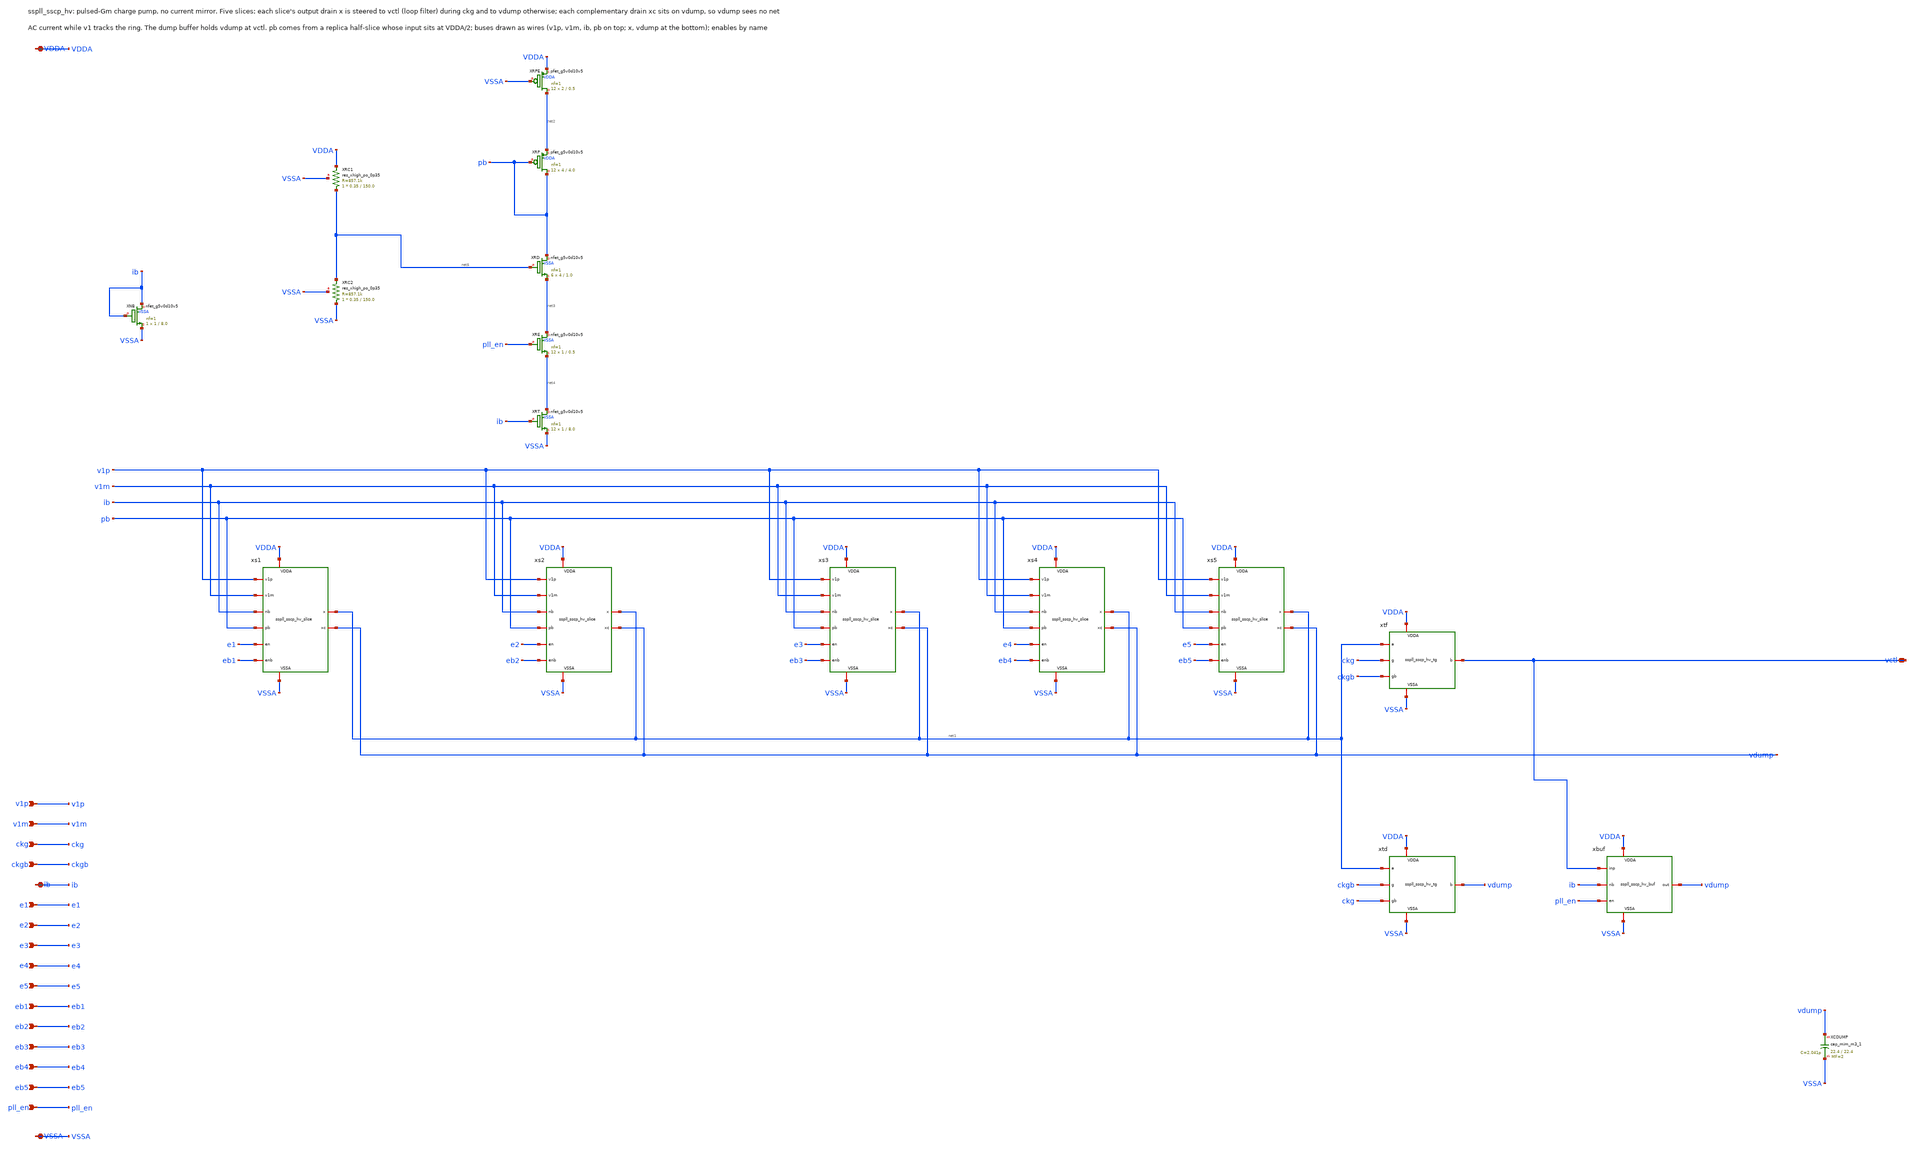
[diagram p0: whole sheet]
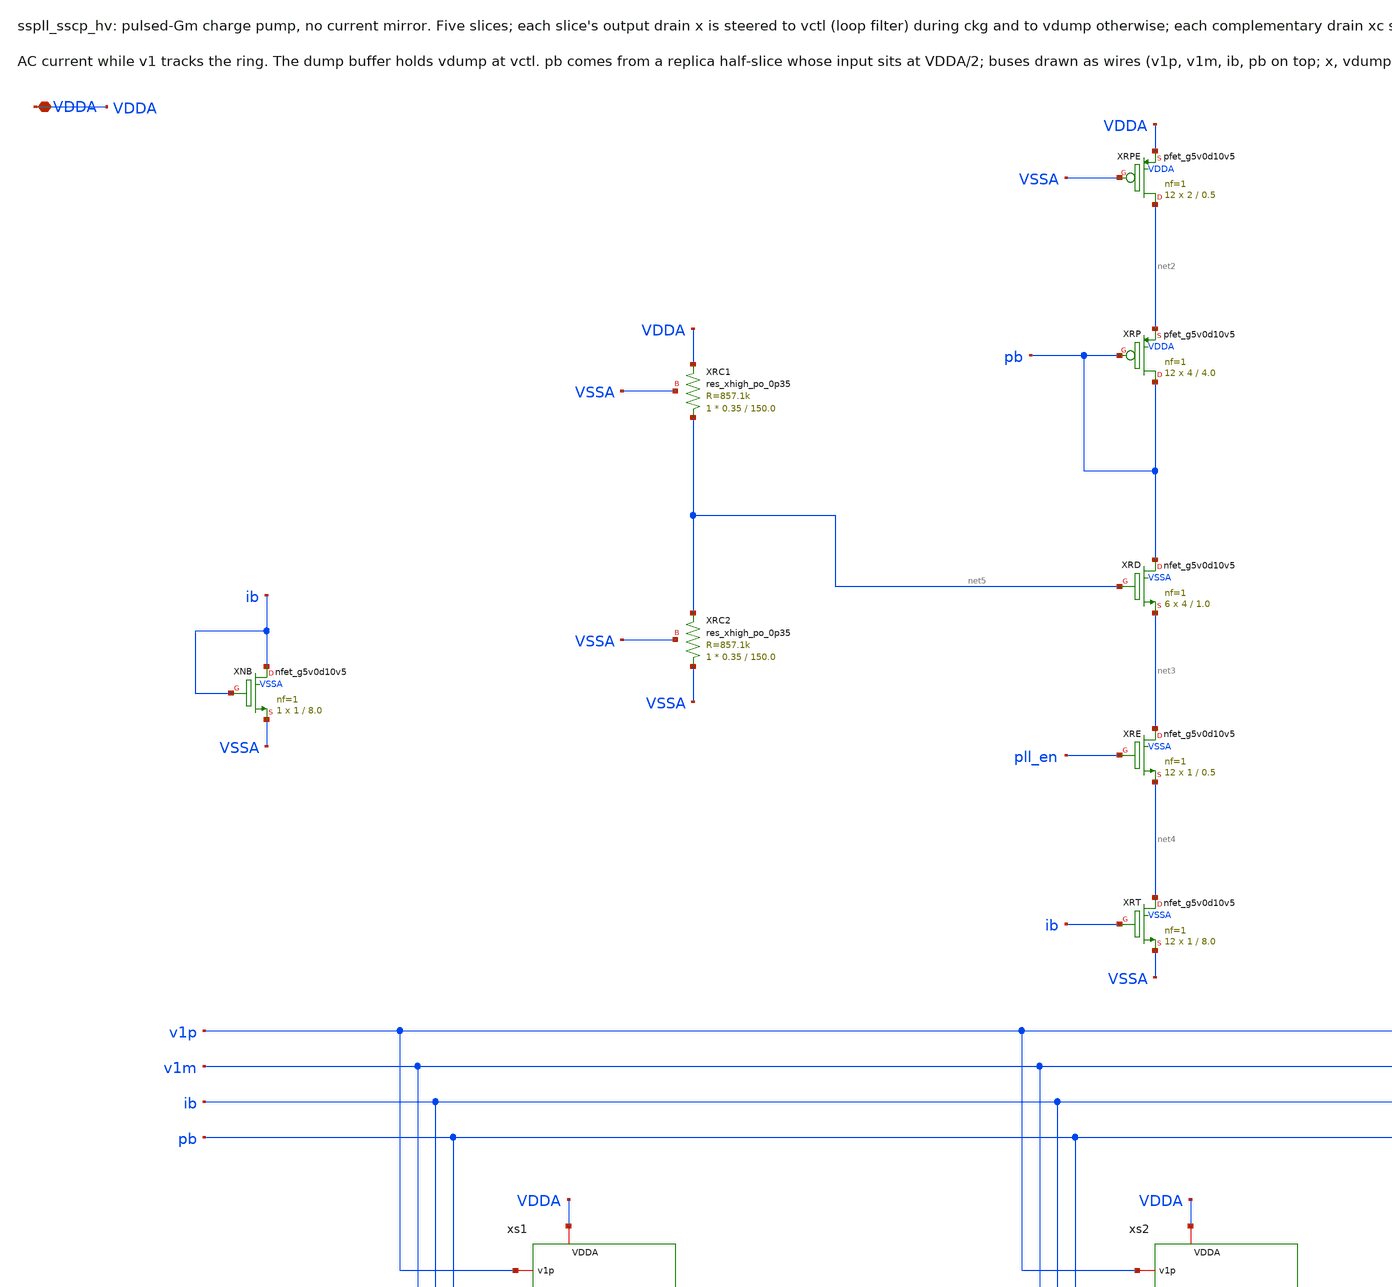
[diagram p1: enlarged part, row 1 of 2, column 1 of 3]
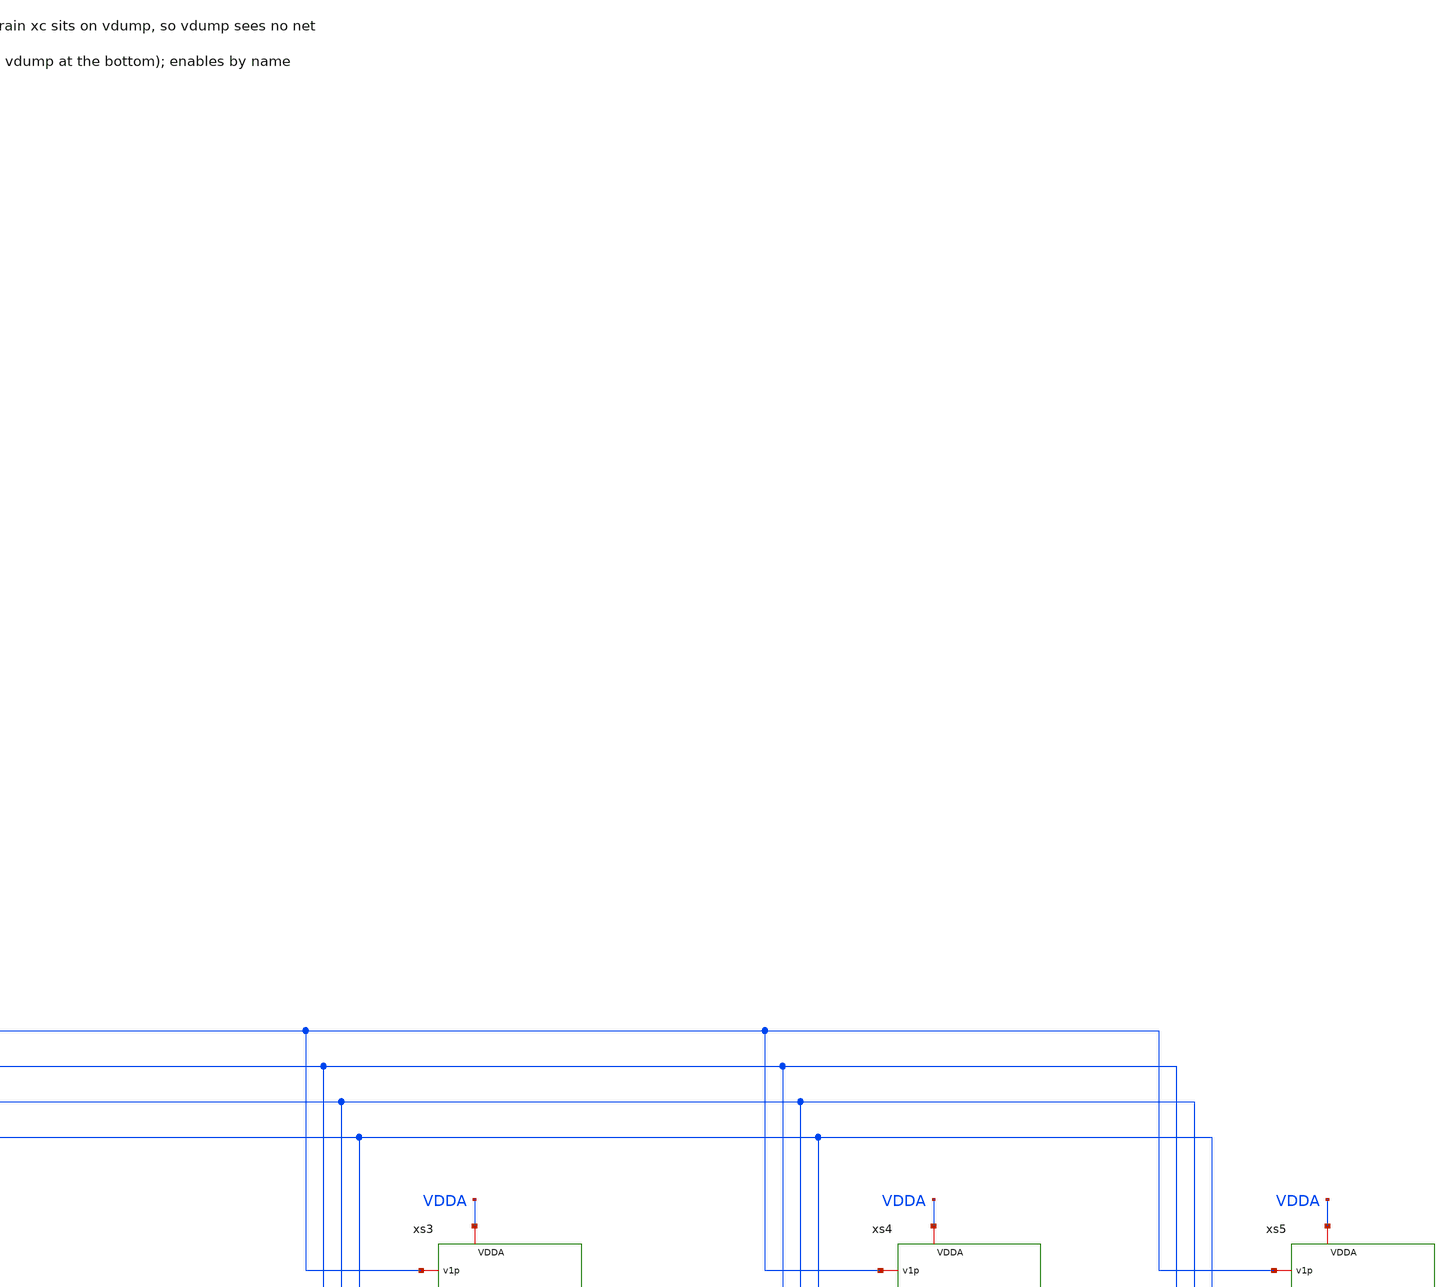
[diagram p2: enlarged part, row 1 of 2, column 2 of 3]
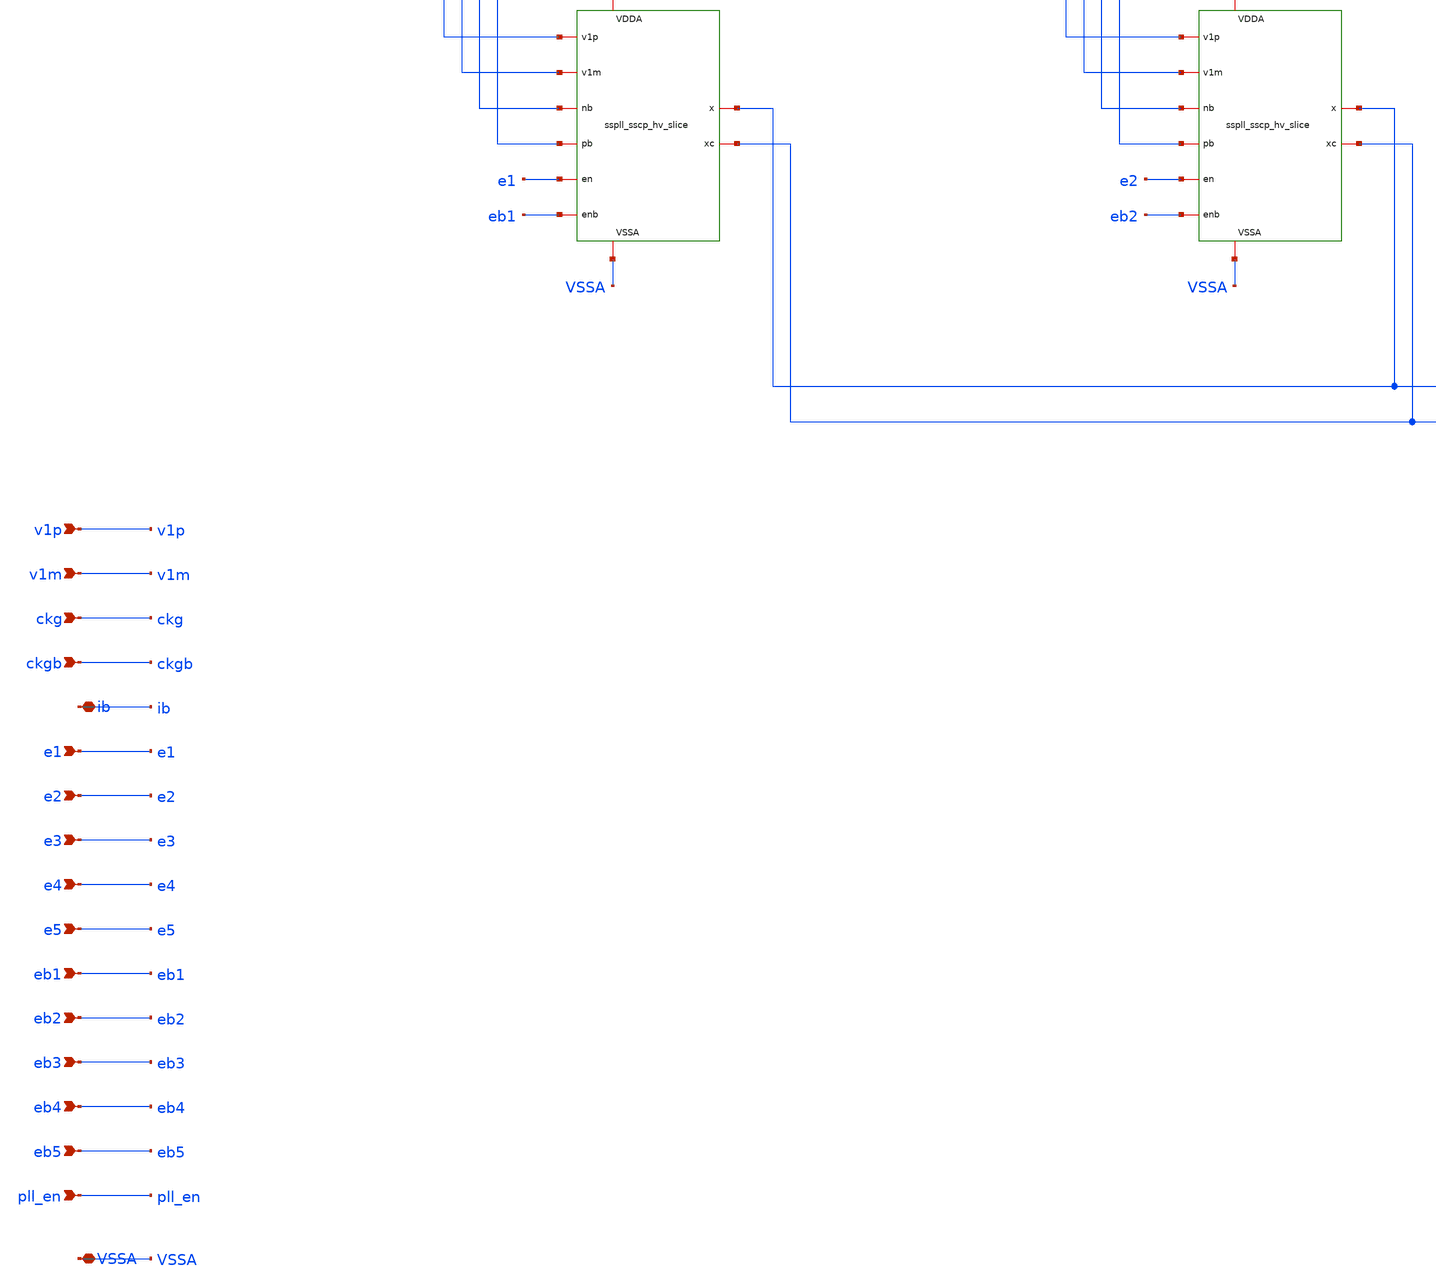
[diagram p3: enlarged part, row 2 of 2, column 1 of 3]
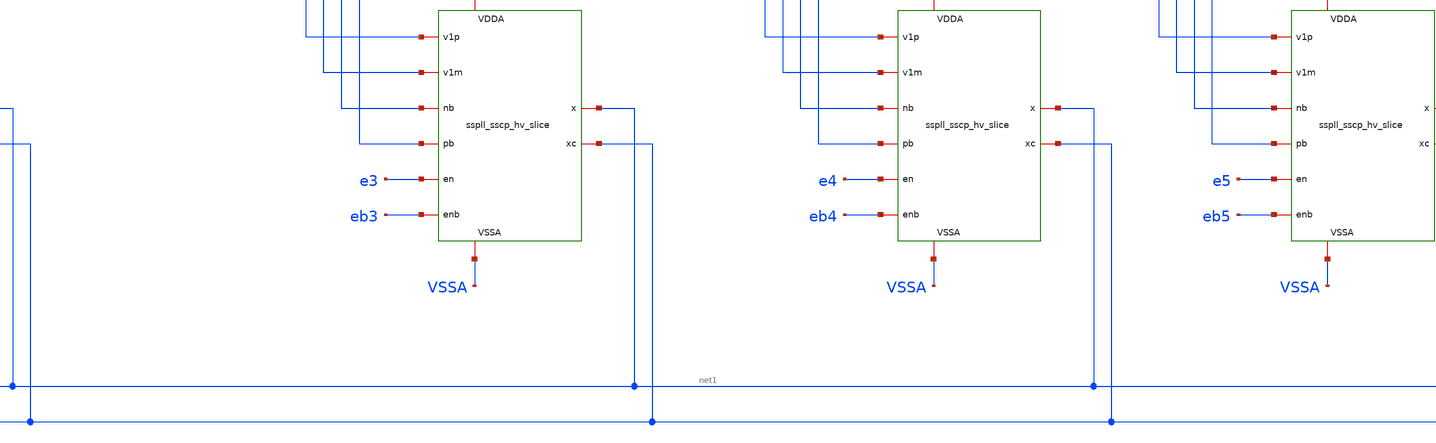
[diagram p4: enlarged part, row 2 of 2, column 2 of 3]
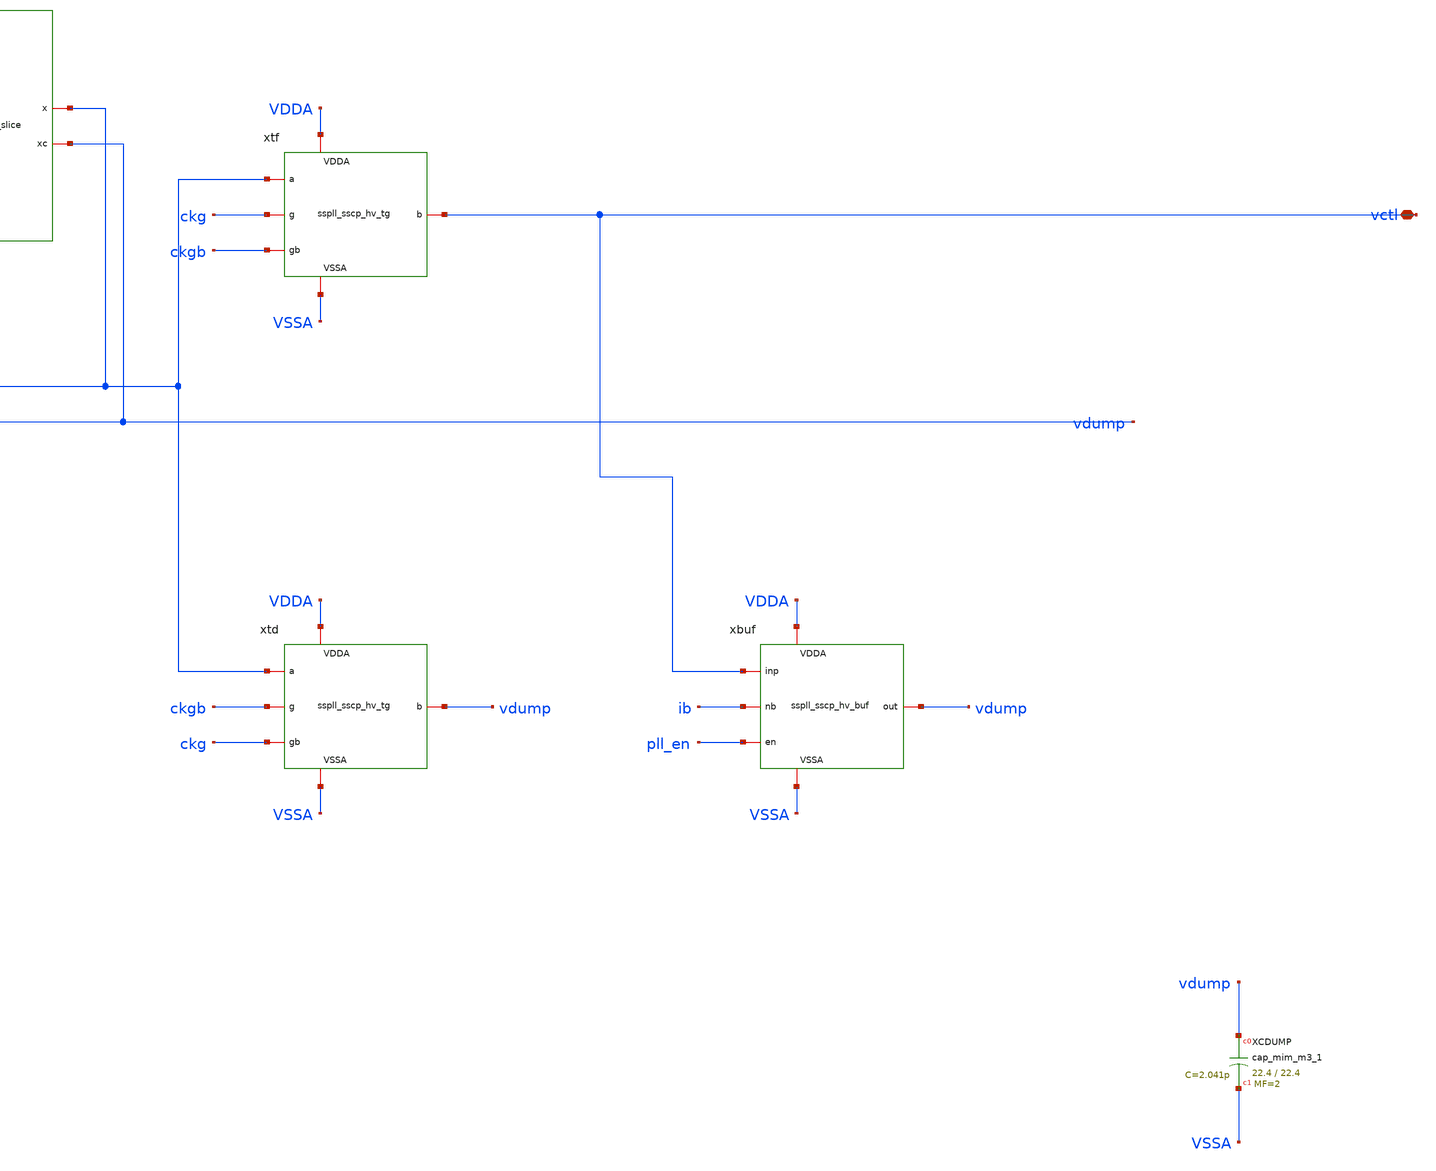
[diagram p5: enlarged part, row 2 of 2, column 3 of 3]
** sch_path: xschem/sscp_hv/sspll_sscp_hv.sch
**.subckt sspll_sscp_hv vctl v1p v1m ckg ckgb ib e1 e2 e3 e4 e5 eb1 eb2 eb3 eb4 eb5 pll_en VDDA VSSA
*.iopin vctl
*.ipin v1p
*.ipin v1m
*.ipin ckg
*.ipin ckgb
*.iopin ib
*.ipin e1
*.ipin e2
*.ipin e3
*.ipin e4
*.ipin e5
*.ipin eb1
*.ipin eb2
*.ipin eb3
*.ipin eb4
*.ipin eb5
*.ipin pll_en
*.iopin VDDA
*.iopin VSSA
xs1 v1p v1m ib pb e1 eb1 net1 vdump VDDA VSSA sspll_sscp_hv_slice
xs2 v1p v1m ib pb e2 eb2 net1 vdump VDDA VSSA sspll_sscp_hv_slice
xs3 v1p v1m ib pb e3 eb3 net1 vdump VDDA VSSA sspll_sscp_hv_slice
xs4 v1p v1m ib pb e4 eb4 net1 vdump VDDA VSSA sspll_sscp_hv_slice
xs5 v1p v1m ib pb e5 eb5 net1 vdump VDDA VSSA sspll_sscp_hv_slice
xtf net1 ckg ckgb vctl VDDA VSSA sspll_sscp_hv_tg
xtd net1 ckgb ckg vdump VDDA VSSA sspll_sscp_hv_tg
xbuf vctl ib pll_en vdump VDDA VSSA sspll_sscp_hv_buf
XXCDUMP vdump VSSA sky130_fd_pr__cap_mim_m3_1 W=22.4 L=22.4 MF=2 m=2
XXNB ib ib VSSA VSSA sky130_fd_pr__nfet_g5v0d10v5 L=8.0 W=1 nf=1 ad='int((nf+1)/2) * W/nf * 0.29' as='int((nf+2)/2) * W/nf * 0.29'
+ pd='2*int((nf+1)/2) * (W/nf + 0.29)' ps='2*int((nf+2)/2) * (W/nf + 0.29)' nrd='0.29 / W' nrs='0.29 / W'
+ sa=0 sb=0 sd=0 mult=1 m=1
XXRPE net2 VSSA VDDA VDDA sky130_fd_pr__pfet_g5v0d10v5 L=0.5 W=2 nf=1 ad='int((nf+1)/2) * W/nf * 0.29'
+ as='int((nf+2)/2) * W/nf * 0.29' pd='2*int((nf+1)/2) * (W/nf + 0.29)' ps='2*int((nf+2)/2) * (W/nf + 0.29)'
+ nrd='0.29 / W' nrs='0.29 / W' sa=0 sb=0 sd=0 mult=12 m=12
XXRP pb pb net2 VDDA sky130_fd_pr__pfet_g5v0d10v5 L=4.0 W=4 nf=1 ad='int((nf+1)/2) * W/nf * 0.29' as='int((nf+2)/2) * W/nf * 0.29'
+ pd='2*int((nf+1)/2) * (W/nf + 0.29)' ps='2*int((nf+2)/2) * (W/nf + 0.29)' nrd='0.29 / W' nrs='0.29 / W'
+ sa=0 sb=0 sd=0 mult=12 m=12
XXRD pb net5 net3 VSSA sky130_fd_pr__nfet_g5v0d10v5 L=1.0 W=4 nf=1 ad='int((nf+1)/2) * W/nf * 0.29' as='int((nf+2)/2) * W/nf * 0.29'
+ pd='2*int((nf+1)/2) * (W/nf + 0.29)' ps='2*int((nf+2)/2) * (W/nf + 0.29)' nrd='0.29 / W' nrs='0.29 / W'
+ sa=0 sb=0 sd=0 mult=6 m=6
XXRE net3 pll_en net4 VSSA sky130_fd_pr__nfet_g5v0d10v5 L=0.5 W=1 nf=1 ad='int((nf+1)/2) * W/nf * 0.29'
+ as='int((nf+2)/2) * W/nf * 0.29' pd='2*int((nf+1)/2) * (W/nf + 0.29)' ps='2*int((nf+2)/2) * (W/nf + 0.29)'
+ nrd='0.29 / W' nrs='0.29 / W' sa=0 sb=0 sd=0 mult=12 m=12
XXRT net4 ib VSSA VSSA sky130_fd_pr__nfet_g5v0d10v5 L=8.0 W=1 nf=1 ad='int((nf+1)/2) * W/nf * 0.29' as='int((nf+2)/2) * W/nf * 0.29'
+ pd='2*int((nf+1)/2) * (W/nf + 0.29)' ps='2*int((nf+2)/2) * (W/nf + 0.29)' nrd='0.29 / W' nrs='0.29 / W'
+ sa=0 sb=0 sd=0 mult=12 m=12
XXRC1 net5 VDDA VSSA sky130_fd_pr__res_xhigh_po_0p35 L=150.0 mult=1 m=1
XXRC2 VSSA net5 VSSA sky130_fd_pr__res_xhigh_po_0p35 L=150.0 mult=1 m=1
**.ends

* expanding   symbol:  sspll_sscp_hv_slice.sym # of pins=10
** sym_path: xschem/sscp_hv/sspll_sscp_hv_slice.sym
** sch_path: xschem/sscp_hv/sspll_sscp_hv_slice.sch
.subckt sspll_sscp_hv_slice v1p v1m nb pb en enb x xc VDDA VSSA
*.ipin v1p
*.ipin v1m
*.ipin nb
*.ipin pb
*.ipin en
*.ipin enb
*.iopin x
*.iopin xc
*.iopin VDDA
*.iopin VSSA
XXPE1 net1 enb VDDA VDDA sky130_fd_pr__pfet_g5v0d10v5 L=0.5 W=2 nf=1 ad='int((nf+1)/2) * W/nf * 0.29'
+ as='int((nf+2)/2) * W/nf * 0.29' pd='2*int((nf+1)/2) * (W/nf + 0.29)' ps='2*int((nf+2)/2) * (W/nf + 0.29)'
+ nrd='0.29 / W' nrs='0.29 / W' sa=0 sb=0 sd=0 mult=2 m=2
XXPE2 net2 enb VDDA VDDA sky130_fd_pr__pfet_g5v0d10v5 L=0.5 W=2 nf=1 ad='int((nf+1)/2) * W/nf * 0.29'
+ as='int((nf+2)/2) * W/nf * 0.29' pd='2*int((nf+1)/2) * (W/nf + 0.29)' ps='2*int((nf+2)/2) * (W/nf + 0.29)'
+ nrd='0.29 / W' nrs='0.29 / W' sa=0 sb=0 sd=0 mult=2 m=2
XXPC xc pb net1 VDDA sky130_fd_pr__pfet_g5v0d10v5 L=4.0 W=4 nf=1 ad='int((nf+1)/2) * W/nf * 0.29' as='int((nf+2)/2) * W/nf * 0.29'
+ pd='2*int((nf+1)/2) * (W/nf + 0.29)' ps='2*int((nf+2)/2) * (W/nf + 0.29)' nrd='0.29 / W' nrs='0.29 / W'
+ sa=0 sb=0 sd=0 mult=2 m=2
XXPX x pb net2 VDDA sky130_fd_pr__pfet_g5v0d10v5 L=4.0 W=4 nf=1 ad='int((nf+1)/2) * W/nf * 0.29' as='int((nf+2)/2) * W/nf * 0.29'
+ pd='2*int((nf+1)/2) * (W/nf + 0.29)' ps='2*int((nf+2)/2) * (W/nf + 0.29)' nrd='0.29 / W' nrs='0.29 / W'
+ sa=0 sb=0 sd=0 mult=2 m=2
XXN1 xc v1p net3 VSSA sky130_fd_pr__nfet_g5v0d10v5 L=1.0 W=4 nf=1 ad='int((nf+1)/2) * W/nf * 0.29' as='int((nf+2)/2) * W/nf * 0.29'
+ pd='2*int((nf+1)/2) * (W/nf + 0.29)' ps='2*int((nf+2)/2) * (W/nf + 0.29)' nrd='0.29 / W' nrs='0.29 / W'
+ sa=0 sb=0 sd=0 mult=1 m=1
XXN2 x v1m net4 VSSA sky130_fd_pr__nfet_g5v0d10v5 L=1.0 W=4 nf=1 ad='int((nf+1)/2) * W/nf * 0.29' as='int((nf+2)/2) * W/nf * 0.29'
+ pd='2*int((nf+1)/2) * (W/nf + 0.29)' ps='2*int((nf+2)/2) * (W/nf + 0.29)' nrd='0.29 / W' nrs='0.29 / W'
+ sa=0 sb=0 sd=0 mult=1 m=1
xrs net3 net4 VSSA sspll_sscp_hv_rs
XXE1 net3 en net5 VSSA sky130_fd_pr__nfet_g5v0d10v5 L=0.5 W=1 nf=1 ad='int((nf+1)/2) * W/nf * 0.29' as='int((nf+2)/2) * W/nf * 0.29'
+ pd='2*int((nf+1)/2) * (W/nf + 0.29)' ps='2*int((nf+2)/2) * (W/nf + 0.29)' nrd='0.29 / W' nrs='0.29 / W'
+ sa=0 sb=0 sd=0 mult=2 m=2
XXE2 net4 en net6 VSSA sky130_fd_pr__nfet_g5v0d10v5 L=0.5 W=1 nf=1 ad='int((nf+1)/2) * W/nf * 0.29' as='int((nf+2)/2) * W/nf * 0.29'
+ pd='2*int((nf+1)/2) * (W/nf + 0.29)' ps='2*int((nf+2)/2) * (W/nf + 0.29)' nrd='0.29 / W' nrs='0.29 / W'
+ sa=0 sb=0 sd=0 mult=2 m=2
XXT1 net5 nb VSSA VSSA sky130_fd_pr__nfet_g5v0d10v5 L=8.0 W=1 nf=1 ad='int((nf+1)/2) * W/nf * 0.29' as='int((nf+2)/2) * W/nf * 0.29'
+ pd='2*int((nf+1)/2) * (W/nf + 0.29)' ps='2*int((nf+2)/2) * (W/nf + 0.29)' nrd='0.29 / W' nrs='0.29 / W'
+ sa=0 sb=0 sd=0 mult=2 m=2
XXT2 net6 nb VSSA VSSA sky130_fd_pr__nfet_g5v0d10v5 L=8.0 W=1 nf=1 ad='int((nf+1)/2) * W/nf * 0.29' as='int((nf+2)/2) * W/nf * 0.29'
+ pd='2*int((nf+1)/2) * (W/nf + 0.29)' ps='2*int((nf+2)/2) * (W/nf + 0.29)' nrd='0.29 / W' nrs='0.29 / W'
+ sa=0 sb=0 sd=0 mult=2 m=2
.ends


* expanding   symbol:  sspll_sscp_hv_tg.sym # of pins=6
** sym_path: xschem/sscp_hv/sspll_sscp_hv_tg.sym
** sch_path: xschem/sscp_hv/sspll_sscp_hv_tg.sch
.subckt sspll_sscp_hv_tg a g gb b VDDA VSSA
*.iopin a
*.iopin b
*.ipin g
*.ipin gb
*.iopin VDDA
*.iopin VSSA
XXN a g b VSSA sky130_fd_pr__nfet_g5v0d10v5 L=0.5 W=1 nf=1 ad='int((nf+1)/2) * W/nf * 0.29' as='int((nf+2)/2) * W/nf * 0.29'
+ pd='2*int((nf+1)/2) * (W/nf + 0.29)' ps='2*int((nf+2)/2) * (W/nf + 0.29)' nrd='0.29 / W' nrs='0.29 / W'
+ sa=0 sb=0 sd=0 mult=1 m=1
XXP b gb a VDDA sky130_fd_pr__pfet_g5v0d10v5 L=0.5 W=1 nf=1 ad='int((nf+1)/2) * W/nf * 0.29' as='int((nf+2)/2) * W/nf * 0.29'
+ pd='2*int((nf+1)/2) * (W/nf + 0.29)' ps='2*int((nf+2)/2) * (W/nf + 0.29)' nrd='0.29 / W' nrs='0.29 / W'
+ sa=0 sb=0 sd=0 mult=1 m=1
.ends


* expanding   symbol:  sspll_sscp_hv_buf.sym # of pins=6
** sym_path: xschem/sscp_hv/sspll_sscp_hv_buf.sym
** sch_path: xschem/sscp_hv/sspll_sscp_hv_buf.sch
.subckt sspll_sscp_hv_buf inp nb en out VDDA VSSA
*.ipin inp
*.ipin nb
*.ipin en
*.opin out
*.iopin VDDA
*.iopin VSSA
XXL1 o1 o1 VDDA VDDA sky130_fd_pr__pfet_g5v0d10v5 L=2.0 W=16 nf=1 ad='int((nf+1)/2) * W/nf * 0.29' as='int((nf+2)/2) * W/nf * 0.29'
+ pd='2*int((nf+1)/2) * (W/nf + 0.29)' ps='2*int((nf+2)/2) * (W/nf + 0.29)' nrd='0.29 / W' nrs='0.29 / W'
+ sa=0 sb=0 sd=0 mult=1 m=1
XXL2 out o1 VDDA VDDA sky130_fd_pr__pfet_g5v0d10v5 L=2.0 W=16 nf=1 ad='int((nf+1)/2) * W/nf * 0.29' as='int((nf+2)/2) * W/nf * 0.29'
+ pd='2*int((nf+1)/2) * (W/nf + 0.29)' ps='2*int((nf+2)/2) * (W/nf + 0.29)' nrd='0.29 / W' nrs='0.29 / W'
+ sa=0 sb=0 sd=0 mult=1 m=1
XXA1 o1 inp net1 VSSA sky130_fd_pr__nfet_g5v0d10v5 L=2.0 W=8 nf=1 ad='int((nf+1)/2) * W/nf * 0.29' as='int((nf+2)/2) * W/nf * 0.29'
+ pd='2*int((nf+1)/2) * (W/nf + 0.29)' ps='2*int((nf+2)/2) * (W/nf + 0.29)' nrd='0.29 / W' nrs='0.29 / W'
+ sa=0 sb=0 sd=0 mult=1 m=1
XXA2 out out net1 VSSA sky130_fd_pr__nfet_g5v0d10v5 L=2.0 W=8 nf=1 ad='int((nf+1)/2) * W/nf * 0.29' as='int((nf+2)/2) * W/nf * 0.29'
+ pd='2*int((nf+1)/2) * (W/nf + 0.29)' ps='2*int((nf+2)/2) * (W/nf + 0.29)' nrd='0.29 / W' nrs='0.29 / W'
+ sa=0 sb=0 sd=0 mult=1 m=1
XXBE net1 en net2 VSSA sky130_fd_pr__nfet_g5v0d10v5 L=0.5 W=1 nf=1 ad='int((nf+1)/2) * W/nf * 0.29' as='int((nf+2)/2) * W/nf * 0.29'
+ pd='2*int((nf+1)/2) * (W/nf + 0.29)' ps='2*int((nf+2)/2) * (W/nf + 0.29)' nrd='0.29 / W' nrs='0.29 / W'
+ sa=0 sb=0 sd=0 mult=10 m=10
XXBT net2 nb VSSA VSSA sky130_fd_pr__nfet_g5v0d10v5 L=8.0 W=2 nf=1 ad='int((nf+1)/2) * W/nf * 0.29' as='int((nf+2)/2) * W/nf * 0.29'
+ pd='2*int((nf+1)/2) * (W/nf + 0.29)' ps='2*int((nf+2)/2) * (W/nf + 0.29)' nrd='0.29 / W' nrs='0.29 / W'
+ sa=0 sb=0 sd=0 mult=10 m=10
.ends


* expanding   symbol:  sspll_sscp_hv_rs.sym # of pins=3
** sym_path: xschem/sscp_hv/sspll_sscp_hv_rs.sym
** sch_path: xschem/sscp_hv/sspll_sscp_hv_rs.sch
.subckt sspll_sscp_hv_rs a b VSS
*.iopin a
*.iopin b
*.iopin VSS
XXR0 b a VSS sky130_fd_pr__res_xhigh_po_0p35 L=17.2 mult=1 m=1
.ends

.end
